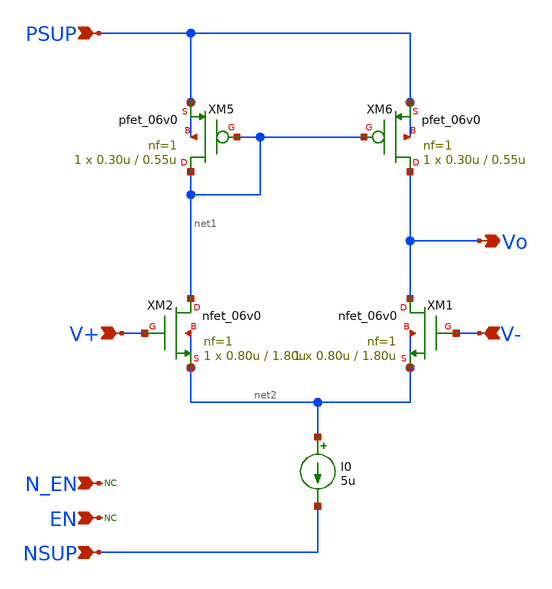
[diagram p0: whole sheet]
** sch_path: xschem/lib/aux_amp.sch
**.subckt aux_amp PSUP NSUP N_EN EN V+ V- Vo
*.ipin PSUP
*.ipin NSUP
*.ipin N_EN
*.ipin EN
*.ipin V+
*.ipin V-
*.opin Vo
XM1 Vo V- net2 net2 nfet_06v0 L=1.80u W=0.80u nf=1 ad='int((nf+1)/2) * W/nf * 0.18u' as='int((nf+2)/2) * W/nf * 0.18u'
+ pd='2*int((nf+1)/2) * (W/nf + 0.18u)' ps='2*int((nf+2)/2) * (W/nf + 0.18u)' nrd='0.18u / W' nrs='0.18u / W'
+ sa=0 sb=0 sd=0 m=1
XM2 net1 V+ net2 net2 nfet_06v0 L=1.80u W=0.80u nf=1 ad='int((nf+1)/2) * W/nf * 0.18u' as='int((nf+2)/2) * W/nf * 0.18u'
+ pd='2*int((nf+1)/2) * (W/nf + 0.18u)' ps='2*int((nf+2)/2) * (W/nf + 0.18u)' nrd='0.18u / W' nrs='0.18u / W'
+ sa=0 sb=0 sd=0 m=1
XM5 net1 net1 PSUP PSUP pfet_06v0 L=0.55u W=0.30u nf=1 ad='int((nf+1)/2) * W/nf * 0.18u' as='int((nf+2)/2) * W/nf * 0.18u'
+ pd='2*int((nf+1)/2) * (W/nf + 0.18u)' ps='2*int((nf+2)/2) * (W/nf + 0.18u)' nrd='0.18u / W' nrs='0.18u / W'
+ sa=0 sb=0 sd=0 m=1
XM6 Vo net1 PSUP PSUP pfet_06v0 L=0.55u W=0.30u nf=1 ad='int((nf+1)/2) * W/nf * 0.18u' as='int((nf+2)/2) * W/nf * 0.18u'
+ pd='2*int((nf+1)/2) * (W/nf + 0.18u)' ps='2*int((nf+2)/2) * (W/nf + 0.18u)' nrd='0.18u / W' nrs='0.18u / W'
+ sa=0 sb=0 sd=0 m=1
I0 net2 NSUP 5u
* noconn N_EN
* noconn EN
**.ends
.end
